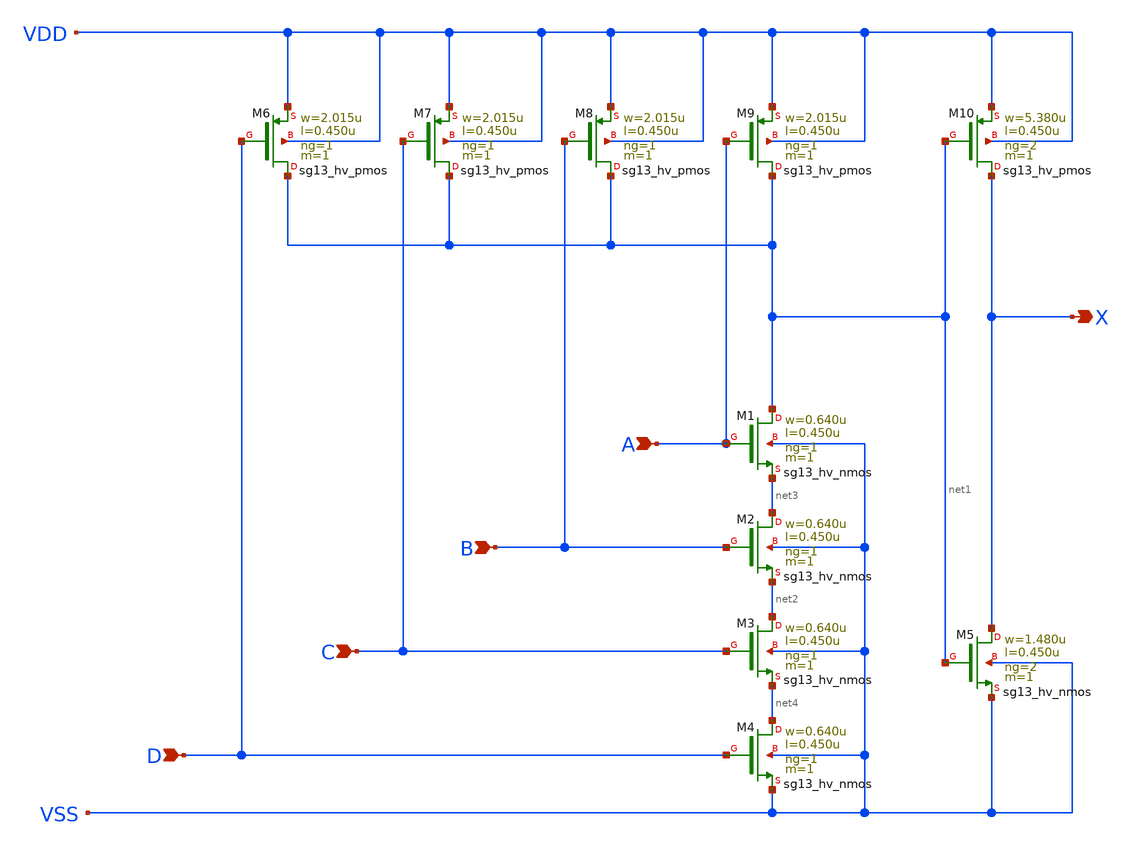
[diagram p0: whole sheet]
** sch_path: ihp-sg13g2/libs.ref/sg13g2_stdcell_hv/sch/xschem/sg13g2_hv_and4_2.sch
* Copyright 2023 IHP PDK Authors
* Licensed under the Apache License, Version 2.0 (the "License");
* you may not use this file except in compliance with the License.
* You may obtain a copy of the License at
* https://www.apache.org/licenses/LICENSE-2.0
* Unless required by applicable law or agreed to in writing, software
* distributed under the License is distributed on an "AS IS" BASIS,
* WITHOUT WARRANTIES OR CONDITIONS OF ANY KIND, either express or implied.
* See the License for the specific language governing permissions and
* limitations under the License.
**.subckt sg13g2_hv_and4_2 A B C D X
*.ipin A
*.ipin B
*.ipin C
*.ipin D
*.opin X
XM1 net1 A net3 VSS sg13_hv_nmos w=0.640u l=0.450u ng=1 m=1 mm_ok=1
XM2 net3 B net2 VSS sg13_hv_nmos w=0.640u l=0.450u ng=1 m=1 mm_ok=1
XM3 net2 C net4 VSS sg13_hv_nmos w=0.640u l=0.450u ng=1 m=1 mm_ok=1
XM4 net4 D VSS VSS sg13_hv_nmos w=0.640u l=0.450u ng=1 m=1 mm_ok=1
XM5 X net1 VSS VSS sg13_hv_nmos w=1.480u l=0.450u ng=2 m=1 mm_ok=1
XM6 net1 D VDD VDD sg13_hv_pmos w=2.015u l=0.450u ng=1 m=1 mm_ok=1
XM7 net1 C VDD VDD sg13_hv_pmos w=2.015u l=0.450u ng=1 m=1 mm_ok=1
XM8 net1 B VDD VDD sg13_hv_pmos w=2.015u l=0.450u ng=1 m=1 mm_ok=1
XM9 net1 A VDD VDD sg13_hv_pmos w=2.015u l=0.450u ng=1 m=1 mm_ok=1
XM10 X net1 VDD VDD sg13_hv_pmos w=5.380u l=0.450u ng=2 m=1 mm_ok=1
**.ends
.end
